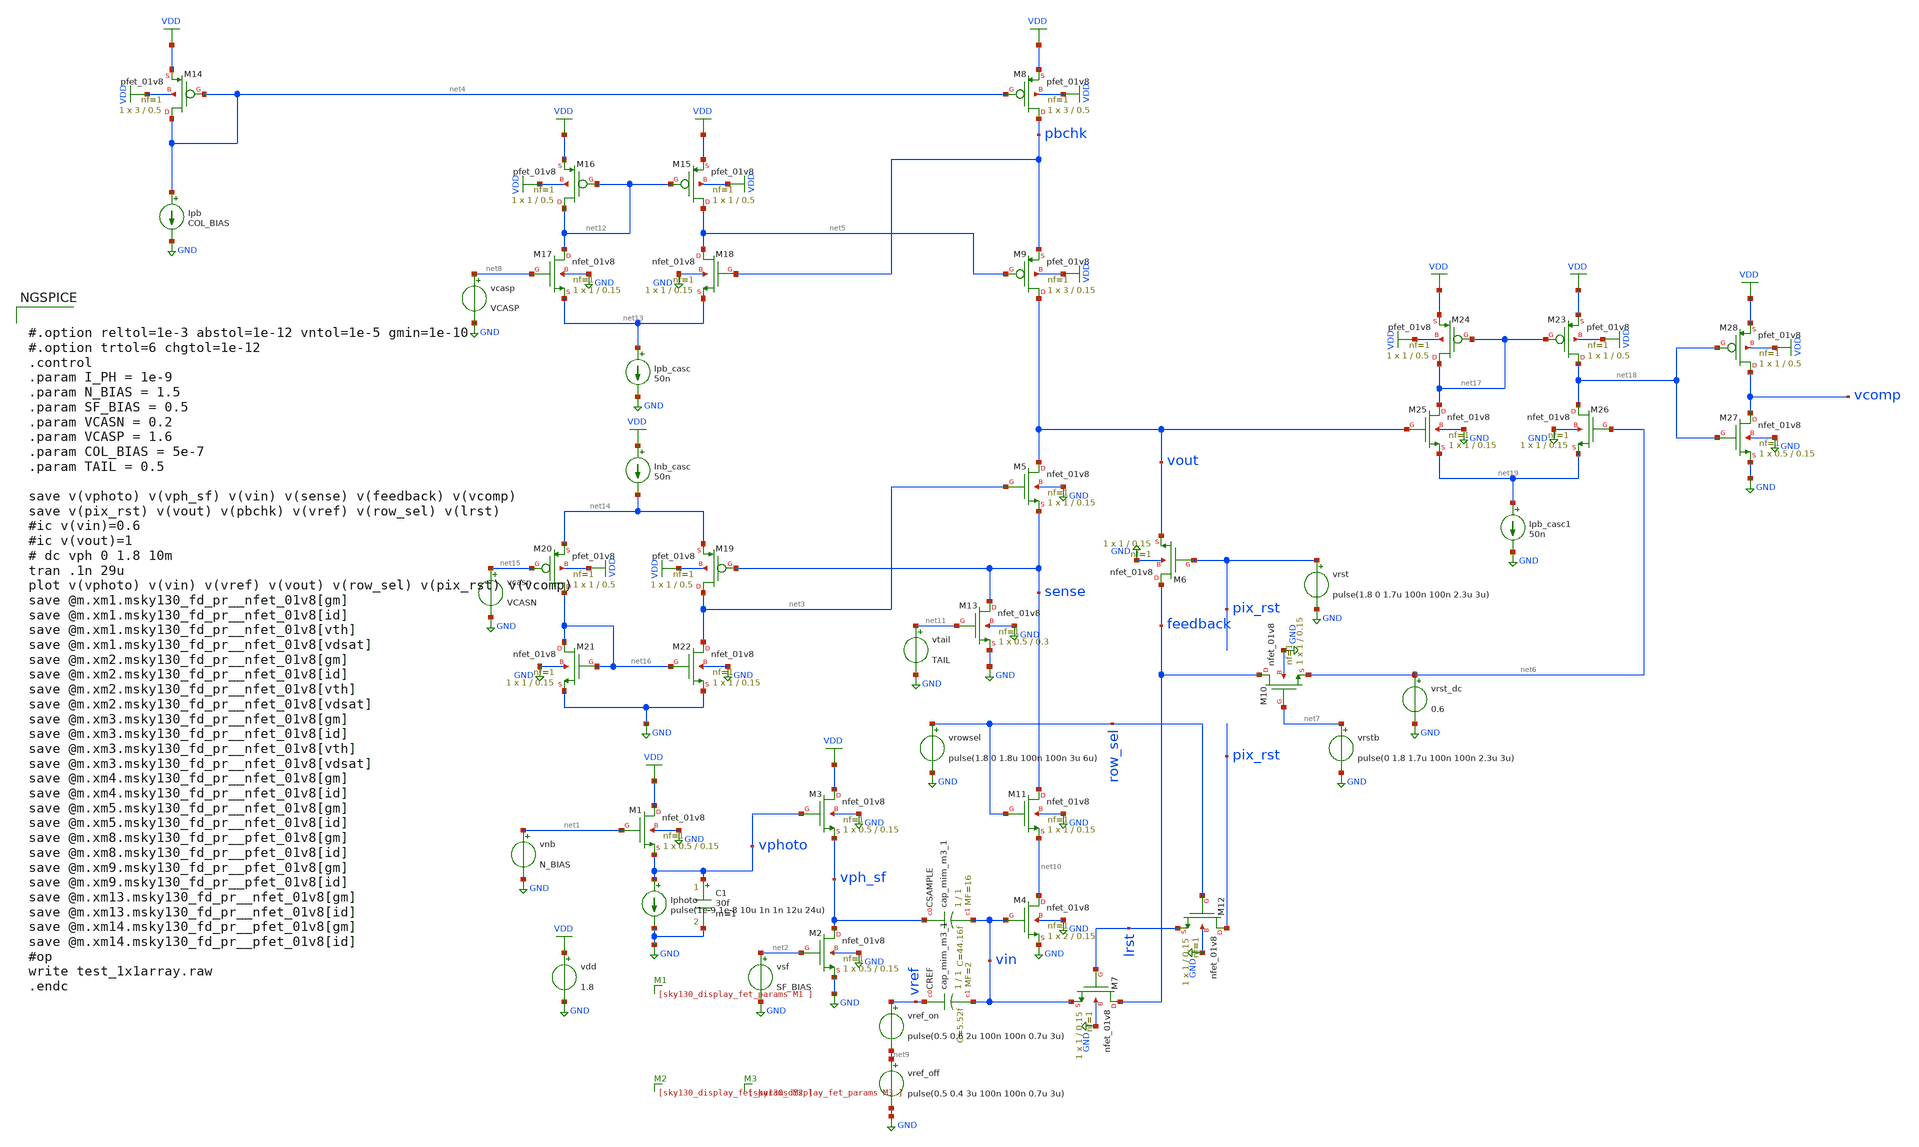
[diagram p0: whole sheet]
** sch_path: analog/klayout/production/final_merge_20260923/testbenches/cace/analog/xschem/test_1x1array_v1_good.sch
**.subckt test_1x1array_v1_good
vdd VDD GND 1.8
.save i(vdd)
XCSAMPLE vph_sf vin sky130_fd_pr__cap_mim_m3_1 W=1 L=1 MF=16 m=16
XCREF vref vin sky130_fd_pr__cap_mim_m3_1 W=1 L=1 MF=2 m=2
C1 vphoto GND 30f m=1
XM1 VDD net1 vphoto GND sky130_fd_pr__nfet_01v8 L=0.15 W=0.5 nf=1 ad='int((1 + 1)/2) * 0.5 / 1 * 0.29'
+ as='int((1 + 2)/2) * 0.5 / 1 * 0.29' pd='2*int((1 + 1)/2) * (0.5 / 1 + 0.29)' ps='2*int((1 + 2)/2) * (0.5 / 1 + 0.29)'
+ nrd='0.29 / 0.5 ' nrs='0.29 / 0.5 ' sa=0 sb=0 sd=0 mult=1 m=1
vnb net1 GND N_BIAS
vsf net2 GND SF_BIAS
vref_on vref net9 pulse(0.5 0.6 2u 100n 100n 0.7u 3u)
Iphoto vphoto GND pulse(1e-9 1e-8 10u 1n 1n 12u 24u)
XM4 net10 vin GND GND sky130_fd_pr__nfet_01v8 L=0.15 W=2 nf=1 ad='int((1 + 1)/2) * 2 / 1 * 0.29' as='int((1 + 2)/2) * 2 / 1 * 0.29'
+ pd='2*int((1 + 1)/2) * (2 / 1 + 0.29)' ps='2*int((1 + 2)/2) * (2 / 1 + 0.29)' nrd='0.29 / 2 ' nrs='0.29 / 2 '
+ sa=0 sb=0 sd=0 mult=1 m=1
XM5 vout net3 sense GND sky130_fd_pr__nfet_01v8 L=0.15 W=1 nf=1 ad='int((1 + 1)/2) * 1 / 1 * 0.29' as='int((1 + 2)/2) * 1 / 1 * 0.29'
+ pd='2*int((1 + 1)/2) * (1 / 1 + 0.29)' ps='2*int((1 + 2)/2) * (1 / 1 + 0.29)' nrd='0.29 / 1 ' nrs='0.29 / 1 '
+ sa=0 sb=0 sd=0 mult=1 m=1
vcasn net15 GND VCASN
XM6 feedback pix_rst vout GND sky130_fd_pr__nfet_01v8 L=0.15 W=1 nf=1 ad='int((1 + 1)/2) * 1 / 1 * 0.29'
+ as='int((1 + 2)/2) * 1 / 1 * 0.29' pd='2*int((1 + 1)/2) * (1 / 1 + 0.29)' ps='2*int((1 + 2)/2) * (1 / 1 + 0.29)'
+ nrd='0.29 / 1 ' nrs='0.29 / 1 ' sa=0 sb=0 sd=0 mult=1 m=1
XM7 feedback lrst vin GND sky130_fd_pr__nfet_01v8 L=0.15 W=1 nf=1 ad='int((1 + 1)/2) * 1 / 1 * 0.29'
+ as='int((1 + 2)/2) * 1 / 1 * 0.29' pd='2*int((1 + 1)/2) * (1 / 1 + 0.29)' ps='2*int((1 + 2)/2) * (1 / 1 + 0.29)'
+ nrd='0.29 / 1 ' nrs='0.29 / 1 ' sa=0 sb=0 sd=0 mult=1 m=1
vrst pix_rst GND pulse(1.8 0 1.7u 100n 100n 2.3u 3u)
Ipb net4 GND COL_BIAS
XM8 pbchk net4 VDD VDD sky130_fd_pr__pfet_01v8 L=0.5 W=3 nf=1 ad='int((1 + 1)/2) * 3 / 1 * 0.29' as='int((1 + 2)/2) * 3 / 1 * 0.29'
+ pd='2*int((1 + 1)/2) * (3 / 1 + 0.29)' ps='2*int((1 + 2)/2) * (3 / 1 + 0.29)' nrd='0.29 / 3 ' nrs='0.29 / 3 '
+ sa=0 sb=0 sd=0 mult=1 m=1
XM9 vout net5 pbchk VDD sky130_fd_pr__pfet_01v8 L=0.15 W=3 nf=1 ad='int((1 + 1)/2) * 3 / 1 * 0.29' as='int((1 + 2)/2) * 3 / 1 * 0.29'
+ pd='2*int((1 + 1)/2) * (3 / 1 + 0.29)' ps='2*int((1 + 2)/2) * (3 / 1 + 0.29)' nrd='0.29 / 3 ' nrs='0.29 / 3 '
+ sa=0 sb=0 sd=0 mult=1 m=1
vcasp net8 GND VCASP
XM10 feedback net7 net6 GND sky130_fd_pr__nfet_01v8 L=0.15 W=1 nf=1 ad='int((1 + 1)/2) * 1 / 1 * 0.29'
+ as='int((1 + 2)/2) * 1 / 1 * 0.29' pd='2*int((1 + 1)/2) * (1 / 1 + 0.29)' ps='2*int((1 + 2)/2) * (1 / 1 + 0.29)'
+ nrd='0.29 / 1 ' nrs='0.29 / 1 ' sa=0 sb=0 sd=0 mult=1 m=1
vrstb net7 GND pulse(0 1.8 1.7u 100n 100n 2.3u 3u)
vrst_dc net6 GND 0.6
vref_off net9 GND pulse(0.5 0.4 3u 100n 100n 0.7u 3u)
XM2 vph_sf net2 GND GND sky130_fd_pr__nfet_01v8 L=0.15 W=0.5 nf=1 ad='int((1 + 1)/2) * 0.5 / 1 * 0.29'
+ as='int((1 + 2)/2) * 0.5 / 1 * 0.29' pd='2*int((1 + 1)/2) * (0.5 / 1 + 0.29)' ps='2*int((1 + 2)/2) * (0.5 / 1 + 0.29)'
+ nrd='0.29 / 0.5 ' nrs='0.29 / 0.5 ' sa=0 sb=0 sd=0 mult=1 m=1
XM3 VDD vphoto vph_sf GND sky130_fd_pr__nfet_01v8 L=0.15 W=0.5 nf=1 ad='int((1 + 1)/2) * 0.5 / 1 * 0.29'
+ as='int((1 + 2)/2) * 0.5 / 1 * 0.29' pd='2*int((1 + 1)/2) * (0.5 / 1 + 0.29)' ps='2*int((1 + 2)/2) * (0.5 / 1 + 0.29)'
+ nrd='0.29 / 0.5 ' nrs='0.29 / 0.5 ' sa=0 sb=0 sd=0 mult=1 m=1
XM11 sense row_sel net10 GND sky130_fd_pr__nfet_01v8 L=0.15 W=1 nf=1 ad='int((1 + 1)/2) * 1 / 1 * 0.29'
+ as='int((1 + 2)/2) * 1 / 1 * 0.29' pd='2*int((1 + 1)/2) * (1 / 1 + 0.29)' ps='2*int((1 + 2)/2) * (1 / 1 + 0.29)'
+ nrd='0.29 / 1 ' nrs='0.29 / 1 ' sa=0 sb=0 sd=0 mult=1 m=1
XM12 pix_rst row_sel lrst GND sky130_fd_pr__nfet_01v8 L=0.15 W=1 nf=1 ad='int((1 + 1)/2) * 1 / 1 * 0.29'
+ as='int((1 + 2)/2) * 1 / 1 * 0.29' pd='2*int((1 + 1)/2) * (1 / 1 + 0.29)' ps='2*int((1 + 2)/2) * (1 / 1 + 0.29)'
+ nrd='0.29 / 1 ' nrs='0.29 / 1 ' sa=0 sb=0 sd=0 mult=1 m=1
vrowsel row_sel GND pulse(1.8 0 1.8u 100n 100n 3u 6u)
vtail net11 GND TAIL
XM13 sense net11 GND GND sky130_fd_pr__nfet_01v8 L=0.3 W=0.5 nf=1 ad='int((1 + 1)/2) * 0.5 / 1 * 0.29'
+ as='int((1 + 2)/2) * 0.5 / 1 * 0.29' pd='2*int((1 + 1)/2) * (0.5 / 1 + 0.29)' ps='2*int((1 + 2)/2) * (0.5 / 1 + 0.29)'
+ nrd='0.29 / 0.5 ' nrs='0.29 / 0.5 ' sa=0 sb=0 sd=0 mult=1 m=1
XM14 net4 net4 VDD VDD sky130_fd_pr__pfet_01v8 L=0.5 W=3 nf=1 ad='int((1 + 1)/2) * 3 / 1 * 0.29' as='int((1 + 2)/2) * 3 / 1 * 0.29'
+ pd='2*int((1 + 1)/2) * (3 / 1 + 0.29)' ps='2*int((1 + 2)/2) * (3 / 1 + 0.29)' nrd='0.29 / 3 ' nrs='0.29 / 3 '
+ sa=0 sb=0 sd=0 mult=1 m=1
XM15 net5 net12 VDD VDD sky130_fd_pr__pfet_01v8 L=0.5 W=1 nf=1 ad='int((1 + 1)/2) * 1 / 1 * 0.29' as='int((1 + 2)/2) * 1 / 1 * 0.29'
+ pd='2*int((1 + 1)/2) * (1 / 1 + 0.29)' ps='2*int((1 + 2)/2) * (1 / 1 + 0.29)' nrd='0.29 / 1 ' nrs='0.29 / 1 '
+ sa=0 sb=0 sd=0 mult=1 m=1
XM16 net12 net12 VDD VDD sky130_fd_pr__pfet_01v8 L=0.5 W=1 nf=1 ad='int((1 + 1)/2) * 1 / 1 * 0.29' as='int((1 + 2)/2) * 1 / 1 * 0.29'
+ pd='2*int((1 + 1)/2) * (1 / 1 + 0.29)' ps='2*int((1 + 2)/2) * (1 / 1 + 0.29)' nrd='0.29 / 1 ' nrs='0.29 / 1 '
+ sa=0 sb=0 sd=0 mult=1 m=1
XM17 net12 net8 net13 GND sky130_fd_pr__nfet_01v8 L=0.15 W=1 nf=1 ad='int((1 + 1)/2) * 1 / 1 * 0.29'
+ as='int((1 + 2)/2) * 1 / 1 * 0.29' pd='2*int((1 + 1)/2) * (1 / 1 + 0.29)' ps='2*int((1 + 2)/2) * (1 / 1 + 0.29)'
+ nrd='0.29 / 1 ' nrs='0.29 / 1 ' sa=0 sb=0 sd=0 mult=1 m=1
XM18 net5 pbchk net13 GND sky130_fd_pr__nfet_01v8 L=0.15 W=1 nf=1 ad='int((1 + 1)/2) * 1 / 1 * 0.29'
+ as='int((1 + 2)/2) * 1 / 1 * 0.29' pd='2*int((1 + 1)/2) * (1 / 1 + 0.29)' ps='2*int((1 + 2)/2) * (1 / 1 + 0.29)'
+ nrd='0.29 / 1 ' nrs='0.29 / 1 ' sa=0 sb=0 sd=0 mult=1 m=1
Ipb_casc net13 GND 50n
XM19 net3 sense net14 VDD sky130_fd_pr__pfet_01v8 L=0.5 W=1 nf=1 ad='int((1 + 1)/2) * 1 / 1 * 0.29' as='int((1 + 2)/2) * 1 / 1 * 0.29'
+ pd='2*int((1 + 1)/2) * (1 / 1 + 0.29)' ps='2*int((1 + 2)/2) * (1 / 1 + 0.29)' nrd='0.29 / 1 ' nrs='0.29 / 1 '
+ sa=0 sb=0 sd=0 mult=1 m=1
Inb_casc VDD net14 50n
XM20 net16 net15 net14 VDD sky130_fd_pr__pfet_01v8 L=0.5 W=1 nf=1 ad='int((1 + 1)/2) * 1 / 1 * 0.29'
+ as='int((1 + 2)/2) * 1 / 1 * 0.29' pd='2*int((1 + 1)/2) * (1 / 1 + 0.29)' ps='2*int((1 + 2)/2) * (1 / 1 + 0.29)'
+ nrd='0.29 / 1 ' nrs='0.29 / 1 ' sa=0 sb=0 sd=0 mult=1 m=1
XM21 net16 net16 GND GND sky130_fd_pr__nfet_01v8 L=0.15 W=1 nf=1 ad='int((1 + 1)/2) * 1 / 1 * 0.29' as='int((1 + 2)/2) * 1 / 1 * 0.29'
+ pd='2*int((1 + 1)/2) * (1 / 1 + 0.29)' ps='2*int((1 + 2)/2) * (1 / 1 + 0.29)' nrd='0.29 / 1 ' nrs='0.29 / 1 '
+ sa=0 sb=0 sd=0 mult=1 m=1
XM22 net3 net16 GND GND sky130_fd_pr__nfet_01v8 L=0.15 W=1 nf=1 ad='int((1 + 1)/2) * 1 / 1 * 0.29' as='int((1 + 2)/2) * 1 / 1 * 0.29'
+ pd='2*int((1 + 1)/2) * (1 / 1 + 0.29)' ps='2*int((1 + 2)/2) * (1 / 1 + 0.29)' nrd='0.29 / 1 ' nrs='0.29 / 1 '
+ sa=0 sb=0 sd=0 mult=1 m=1
XM23 net18 net17 VDD VDD sky130_fd_pr__pfet_01v8 L=0.5 W=1 nf=1 ad='int((1 + 1)/2) * 1 / 1 * 0.29' as='int((1 + 2)/2) * 1 / 1 * 0.29'
+ pd='2*int((1 + 1)/2) * (1 / 1 + 0.29)' ps='2*int((1 + 2)/2) * (1 / 1 + 0.29)' nrd='0.29 / 1 ' nrs='0.29 / 1 '
+ sa=0 sb=0 sd=0 mult=1 m=1
XM24 net17 net17 VDD VDD sky130_fd_pr__pfet_01v8 L=0.5 W=1 nf=1 ad='int((1 + 1)/2) * 1 / 1 * 0.29' as='int((1 + 2)/2) * 1 / 1 * 0.29'
+ pd='2*int((1 + 1)/2) * (1 / 1 + 0.29)' ps='2*int((1 + 2)/2) * (1 / 1 + 0.29)' nrd='0.29 / 1 ' nrs='0.29 / 1 '
+ sa=0 sb=0 sd=0 mult=1 m=1
XM25 net17 vout net19 GND sky130_fd_pr__nfet_01v8 L=0.15 W=1 nf=1 ad='int((1 + 1)/2) * 1 / 1 * 0.29'
+ as='int((1 + 2)/2) * 1 / 1 * 0.29' pd='2*int((1 + 1)/2) * (1 / 1 + 0.29)' ps='2*int((1 + 2)/2) * (1 / 1 + 0.29)'
+ nrd='0.29 / 1 ' nrs='0.29 / 1 ' sa=0 sb=0 sd=0 mult=1 m=1
XM26 net18 net6 net19 GND sky130_fd_pr__nfet_01v8 L=0.15 W=1 nf=1 ad='int((1 + 1)/2) * 1 / 1 * 0.29'
+ as='int((1 + 2)/2) * 1 / 1 * 0.29' pd='2*int((1 + 1)/2) * (1 / 1 + 0.29)' ps='2*int((1 + 2)/2) * (1 / 1 + 0.29)'
+ nrd='0.29 / 1 ' nrs='0.29 / 1 ' sa=0 sb=0 sd=0 mult=1 m=1
Ipb_casc1 net19 GND 50n
XM27 vcomp net18 GND GND sky130_fd_pr__nfet_01v8 L=0.15 W=0.5 nf=1 ad='int((1 + 1)/2) * 0.5 / 1 * 0.29'
+ as='int((1 + 2)/2) * 0.5 / 1 * 0.29' pd='2*int((1 + 1)/2) * (0.5 / 1 + 0.29)' ps='2*int((1 + 2)/2) * (0.5 / 1 + 0.29)'
+ nrd='0.29 / 0.5 ' nrs='0.29 / 0.5 ' sa=0 sb=0 sd=0 mult=1 m=1
XM28 vcomp net18 VDD VDD sky130_fd_pr__pfet_01v8 L=0.5 W=1 nf=1 ad='int((1 + 1)/2) * 1 / 1 * 0.29' as='int((1 + 2)/2) * 1 / 1 * 0.29'
+ pd='2*int((1 + 1)/2) * (1 / 1 + 0.29)' ps='2*int((1 + 2)/2) * (1 / 1 + 0.29)' nrd='0.29 / 1 ' nrs='0.29 / 1 '
+ sa=0 sb=0 sd=0 mult=1 m=1
**** begin user architecture code

** opencircuitdesign pdks install
.lib $::SKYWATER_MODELS/sky130.lib.spice tt



#.option reltol=1e-3 abstol=1e-12 vntol=1e-5 gmin=1e-10
#.option trtol=6 chgtol=1e-12
.control
.param I_PH = 1e-9
.param N_BIAS = 1.5
.param SF_BIAS = 0.5
.param VCASN = 0.2
.param VCASP = 1.6
.param COL_BIAS = 5e-7
.param TAIL = 0.5

save v(vphoto) v(vph_sf) v(vin) v(sense) v(feedback) v(vcomp)
save v(pix_rst) v(vout) v(pbchk) v(vref) v(row_sel) v(lrst)
#ic v(vin)=0.6
#ic v(vout)=1
# dc vph 0 1.8 10m
tran .1n 29u
plot v(vphoto) v(vin) v(vref) v(vout) v(row_sel) v(pix_rst) v(vcomp)
save @m.xm1.msky130_fd_pr__nfet_01v8[gm]
save @m.xm1.msky130_fd_pr__nfet_01v8[id]
save @m.xm1.msky130_fd_pr__nfet_01v8[vth]
save @m.xm1.msky130_fd_pr__nfet_01v8[vdsat]
save @m.xm2.msky130_fd_pr__nfet_01v8[gm]
save @m.xm2.msky130_fd_pr__nfet_01v8[id]
save @m.xm2.msky130_fd_pr__nfet_01v8[vth]
save @m.xm2.msky130_fd_pr__nfet_01v8[vdsat]
save @m.xm3.msky130_fd_pr__nfet_01v8[gm]
save @m.xm3.msky130_fd_pr__nfet_01v8[id]
save @m.xm3.msky130_fd_pr__nfet_01v8[vth]
save @m.xm3.msky130_fd_pr__nfet_01v8[vdsat]
save @m.xm4.msky130_fd_pr__nfet_01v8[gm]
save @m.xm4.msky130_fd_pr__nfet_01v8[id]
save @m.xm5.msky130_fd_pr__nfet_01v8[gm]
save @m.xm5.msky130_fd_pr__nfet_01v8[id]
save @m.xm8.msky130_fd_pr__pfet_01v8[gm]
save @m.xm8.msky130_fd_pr__pfet_01v8[id]
save @m.xm9.msky130_fd_pr__pfet_01v8[gm]
save @m.xm9.msky130_fd_pr__pfet_01v8[id]
save @m.xm13.msky130_fd_pr__nfet_01v8[gm]
save @m.xm13.msky130_fd_pr__nfet_01v8[id]
save @m.xm14.msky130_fd_pr__pfet_01v8[gm]
save @m.xm14.msky130_fd_pr__pfet_01v8[id]
#op
write test_1x1array.raw
.endc


**** end user architecture code
**.ends
.GLOBAL VDD
.GLOBAL GND
.end
